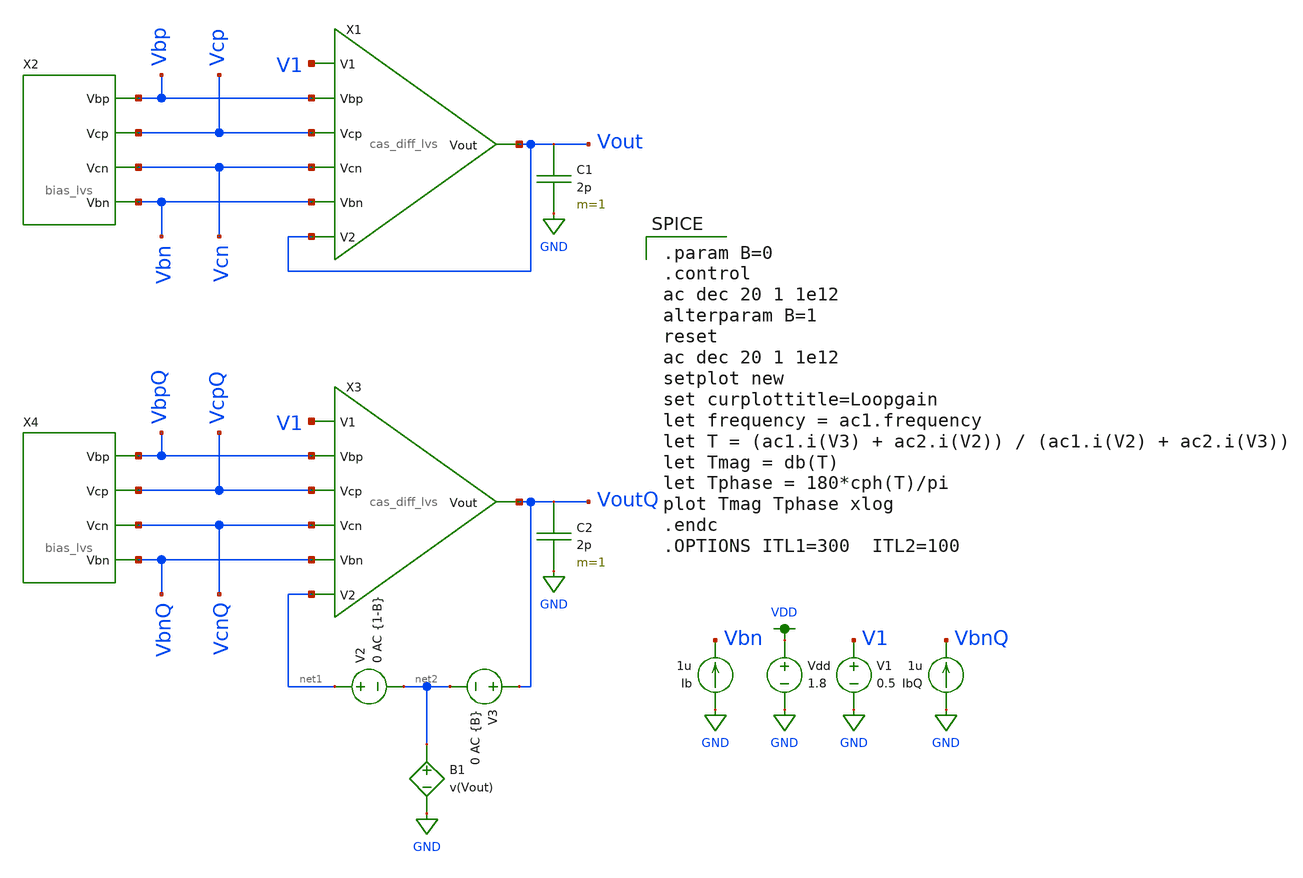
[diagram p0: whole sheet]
** sch_path: mini3/schem/loopgain_noninv.sch
**.subckt loopgain_noninv
X1 V1 Vout Vout Vbp Vcp Vcn Vbn cas_diff_lvs
Vdd VDD GND 1.8
V1 V1 GND 0.5
Ib GND Vbn 1u
C1 Vout GND 2p m=1
X2 Vbp Vcp Vcn Vbn bias_lvs
X3 V1 net1 VoutQ VbpQ VcpQ VcnQ VbnQ cas_diff_lvs
C2 VoutQ GND 2p m=1
X4 VbpQ VcpQ VcnQ VbnQ bias_lvs
IbQ GND VbnQ 1u
V2 net1 net2 0 AC {1-B}
V3 VoutQ net2 0 AC {B}
B1 net2 GND V=v(Vout)
**** begin user architecture code

.option wnflag=1
.lib ~/skywater/skywater-pdk/libraries/sky130_fd_pr_ngspice/latest/models/sky130.lib.spice tt


.param B=0
.control
ac dec 20 1 1e12
alterparam B=1
reset
ac dec 20 1 1e12
setplot new
set curplottitle=Loopgain
let frequency = ac1.frequency
let T = (ac1.i(V3) + ac2.i(V2)) / (ac1.i(V2) + ac2.i(V3))
let Tmag = db(T)
let Tphase = 180*cph(T)/pi
plot Tmag Tphase xlog
.endc
.OPTIONS ITL1=300  ITL2=100

**** end user architecture code
**.ends

* expanding   symbol:  /home/madvlsi/MADVLSI/mini3/schem/cas_diff_lvs.sym # of pins=7
** sym_path: mini3/schem/cas_diff_lvs.sym
** sch_path: mini3/schem/cas_diff_lvs.sch
.subckt cas_diff_lvs V1 V2 Vout Vbp Vcp Vcn Vbn
*.ipin Vbp
*.ipin Vbn
*.ipin Vcn
*.ipin Vcp
*.opin Vout
*.ipin V1
*.ipin V2
XM6a net1 Vcn Vout GND sky130_fd_pr__nfet_01v8 L=0.5 W=6 nf=1 ad='int((nf+1)/2) * W/nf * 0.29' as='int((nf+2)/2) * W/nf * 0.29'
+ pd='2*int((nf+1)/2) * (W/nf + 0.29)' ps='2*int((nf+2)/2) * (W/nf + 0.29)' nrd='0.29 / W' nrs='0.29 / W'
+ sa=0 sb=0 sd=0 mult=1 m=1
XM4a GND Vbn net1 GND sky130_fd_pr__nfet_01v8 L=0.5 W=6 nf=1 ad='int((nf+1)/2) * W/nf * 0.29' as='int((nf+2)/2) * W/nf * 0.29'
+ pd='2*int((nf+1)/2) * (W/nf + 0.29)' ps='2*int((nf+2)/2) * (W/nf + 0.29)' nrd='0.29 / W' nrs='0.29 / W'
+ sa=0 sb=0 sd=0 mult=1 m=1
XM3a net12 Vbn GND GND sky130_fd_pr__nfet_01v8 L=0.5 W=6 nf=1 ad='int((nf+1)/2) * W/nf * 0.29' as='int((nf+2)/2) * W/nf * 0.29'
+ pd='2*int((nf+1)/2) * (W/nf + 0.29)' ps='2*int((nf+2)/2) * (W/nf + 0.29)' nrd='0.29 / W' nrs='0.29 / W'
+ sa=0 sb=0 sd=0 mult=1 m=1
XM5a net2 Vcn net12 GND sky130_fd_pr__nfet_01v8 L=0.5 W=6 nf=1 ad='int((nf+1)/2) * W/nf * 0.29' as='int((nf+2)/2) * W/nf * 0.29'
+ pd='2*int((nf+1)/2) * (W/nf + 0.29)' ps='2*int((nf+2)/2) * (W/nf + 0.29)' nrd='0.29 / W' nrs='0.29 / W'
+ sa=0 sb=0 sd=0 mult=1 m=1
XM5b net12 Vcn net2 GND sky130_fd_pr__nfet_01v8 L=0.5 W=6 nf=1 ad='int((nf+1)/2) * W/nf * 0.29' as='int((nf+2)/2) * W/nf * 0.29'
+ pd='2*int((nf+1)/2) * (W/nf + 0.29)' ps='2*int((nf+2)/2) * (W/nf + 0.29)' nrd='0.29 / W' nrs='0.29 / W'
+ sa=0 sb=0 sd=0 mult=1 m=1
XM3b GND Vbn net12 GND sky130_fd_pr__nfet_01v8 L=0.5 W=6 nf=1 ad='int((nf+1)/2) * W/nf * 0.29' as='int((nf+2)/2) * W/nf * 0.29'
+ pd='2*int((nf+1)/2) * (W/nf + 0.29)' ps='2*int((nf+2)/2) * (W/nf + 0.29)' nrd='0.29 / W' nrs='0.29 / W'
+ sa=0 sb=0 sd=0 mult=1 m=1
XM4b net1 Vbn GND GND sky130_fd_pr__nfet_01v8 L=0.5 W=6 nf=1 ad='int((nf+1)/2) * W/nf * 0.29' as='int((nf+2)/2) * W/nf * 0.29'
+ pd='2*int((nf+1)/2) * (W/nf + 0.29)' ps='2*int((nf+2)/2) * (W/nf + 0.29)' nrd='0.29 / W' nrs='0.29 / W'
+ sa=0 sb=0 sd=0 mult=1 m=1
XM6b Vout Vcn net1 GND sky130_fd_pr__nfet_01v8 L=0.5 W=6 nf=1 ad='int((nf+1)/2) * W/nf * 0.29' as='int((nf+2)/2) * W/nf * 0.29'
+ pd='2*int((nf+1)/2) * (W/nf + 0.29)' ps='2*int((nf+2)/2) * (W/nf + 0.29)' nrd='0.29 / W' nrs='0.29 / W'
+ sa=0 sb=0 sd=0 mult=1 m=1
XM10a Vout Vcp net3 VDD sky130_fd_pr__pfet_01v8 L=0.5 W=6 nf=1 ad='int((nf+1)/2) * W/nf * 0.29' as='int((nf+2)/2) * W/nf * 0.29'
+ pd='2*int((nf+1)/2) * (W/nf + 0.29)' ps='2*int((nf+2)/2) * (W/nf + 0.29)' nrd='0.29 / W' nrs='0.29 / W'
+ sa=0 sb=0 sd=0 mult=1 m=1
XM8a net3 net2 VDD VDD sky130_fd_pr__pfet_01v8 L=0.5 W=6 nf=1 ad='int((nf+1)/2) * W/nf * 0.29' as='int((nf+2)/2) * W/nf * 0.29'
+ pd='2*int((nf+1)/2) * (W/nf + 0.29)' ps='2*int((nf+2)/2) * (W/nf + 0.29)' nrd='0.29 / W' nrs='0.29 / W'
+ sa=0 sb=0 sd=0 mult=1 m=1
XM7a VDD net2 net4 VDD sky130_fd_pr__pfet_01v8 L=0.5 W=6 nf=1 ad='int((nf+1)/2) * W/nf * 0.29' as='int((nf+2)/2) * W/nf * 0.29'
+ pd='2*int((nf+1)/2) * (W/nf + 0.29)' ps='2*int((nf+2)/2) * (W/nf + 0.29)' nrd='0.29 / W' nrs='0.29 / W'
+ sa=0 sb=0 sd=0 mult=1 m=1
XM9a net4 Vcp net2 VDD sky130_fd_pr__pfet_01v8 L=0.5 W=6 nf=1 ad='int((nf+1)/2) * W/nf * 0.29' as='int((nf+2)/2) * W/nf * 0.29'
+ pd='2*int((nf+1)/2) * (W/nf + 0.29)' ps='2*int((nf+2)/2) * (W/nf + 0.29)' nrd='0.29 / W' nrs='0.29 / W'
+ sa=0 sb=0 sd=0 mult=1 m=1
XM9b net2 Vcp net5 VDD sky130_fd_pr__pfet_01v8 L=0.5 W=6 nf=1 ad='int((nf+1)/2) * W/nf * 0.29' as='int((nf+2)/2) * W/nf * 0.29'
+ pd='2*int((nf+1)/2) * (W/nf + 0.29)' ps='2*int((nf+2)/2) * (W/nf + 0.29)' nrd='0.29 / W' nrs='0.29 / W'
+ sa=0 sb=0 sd=0 mult=1 m=1
XM7b net5 net2 VDD VDD sky130_fd_pr__pfet_01v8 L=0.5 W=6 nf=1 ad='int((nf+1)/2) * W/nf * 0.29' as='int((nf+2)/2) * W/nf * 0.29'
+ pd='2*int((nf+1)/2) * (W/nf + 0.29)' ps='2*int((nf+2)/2) * (W/nf + 0.29)' nrd='0.29 / W' nrs='0.29 / W'
+ sa=0 sb=0 sd=0 mult=1 m=1
XM8b VDD net2 net6 VDD sky130_fd_pr__pfet_01v8 L=0.5 W=6 nf=1 ad='int((nf+1)/2) * W/nf * 0.29' as='int((nf+2)/2) * W/nf * 0.29'
+ pd='2*int((nf+1)/2) * (W/nf + 0.29)' ps='2*int((nf+2)/2) * (W/nf + 0.29)' nrd='0.29 / W' nrs='0.29 / W'
+ sa=0 sb=0 sd=0 mult=1 m=1
XM10b net6 Vcp Vout VDD sky130_fd_pr__pfet_01v8 L=0.5 W=6 nf=1 ad='int((nf+1)/2) * W/nf * 0.29' as='int((nf+2)/2) * W/nf * 0.29'
+ pd='2*int((nf+1)/2) * (W/nf + 0.29)' ps='2*int((nf+2)/2) * (W/nf + 0.29)' nrd='0.29 / W' nrs='0.29 / W'
+ sa=0 sb=0 sd=0 mult=1 m=1
XMb1 VDD Vbp net7 VDD sky130_fd_pr__pfet_01v8 L=0.5 W=6 nf=1 ad='int((nf+1)/2) * W/nf * 0.29' as='int((nf+2)/2) * W/nf * 0.29'
+ pd='2*int((nf+1)/2) * (W/nf + 0.29)' ps='2*int((nf+2)/2) * (W/nf + 0.29)' nrd='0.29 / W' nrs='0.29 / W'
+ sa=0 sb=0 sd=0 mult=1 m=1
XMb2 net7 Vbp net8 VDD sky130_fd_pr__pfet_01v8 L=0.5 W=6 nf=1 ad='int((nf+1)/2) * W/nf * 0.29' as='int((nf+2)/2) * W/nf * 0.29'
+ pd='2*int((nf+1)/2) * (W/nf + 0.29)' ps='2*int((nf+2)/2) * (W/nf + 0.29)' nrd='0.29 / W' nrs='0.29 / W'
+ sa=0 sb=0 sd=0 mult=1 m=1
XMb3 net8 Vbp net9 VDD sky130_fd_pr__pfet_01v8 L=0.5 W=6 nf=1 ad='int((nf+1)/2) * W/nf * 0.29' as='int((nf+2)/2) * W/nf * 0.29'
+ pd='2*int((nf+1)/2) * (W/nf + 0.29)' ps='2*int((nf+2)/2) * (W/nf + 0.29)' nrd='0.29 / W' nrs='0.29 / W'
+ sa=0 sb=0 sd=0 mult=1 m=1
XMb4 net9 Vbp VDD VDD sky130_fd_pr__pfet_01v8 L=0.5 W=6 nf=1 ad='int((nf+1)/2) * W/nf * 0.29' as='int((nf+2)/2) * W/nf * 0.29'
+ pd='2*int((nf+1)/2) * (W/nf + 0.29)' ps='2*int((nf+2)/2) * (W/nf + 0.29)' nrd='0.29 / W' nrs='0.29 / W'
+ sa=0 sb=0 sd=0 mult=1 m=1
XMb5 VDD Vbp net10 VDD sky130_fd_pr__pfet_01v8 L=0.5 W=6 nf=1 ad='int((nf+1)/2) * W/nf * 0.29' as='int((nf+2)/2) * W/nf * 0.29'
+ pd='2*int((nf+1)/2) * (W/nf + 0.29)' ps='2*int((nf+2)/2) * (W/nf + 0.29)' nrd='0.29 / W' nrs='0.29 / W'
+ sa=0 sb=0 sd=0 mult=1 m=1
XMb6 net10 Vbp net8 VDD sky130_fd_pr__pfet_01v8 L=0.5 W=6 nf=1 ad='int((nf+1)/2) * W/nf * 0.29' as='int((nf+2)/2) * W/nf * 0.29'
+ pd='2*int((nf+1)/2) * (W/nf + 0.29)' ps='2*int((nf+2)/2) * (W/nf + 0.29)' nrd='0.29 / W' nrs='0.29 / W'
+ sa=0 sb=0 sd=0 mult=1 m=1
XMb7 net8 Vbp net11 VDD sky130_fd_pr__pfet_01v8 L=0.5 W=6 nf=1 ad='int((nf+1)/2) * W/nf * 0.29' as='int((nf+2)/2) * W/nf * 0.29'
+ pd='2*int((nf+1)/2) * (W/nf + 0.29)' ps='2*int((nf+2)/2) * (W/nf + 0.29)' nrd='0.29 / W' nrs='0.29 / W'
+ sa=0 sb=0 sd=0 mult=1 m=1
XMb8 net11 Vbp VDD VDD sky130_fd_pr__pfet_01v8 L=0.5 W=6 nf=1 ad='int((nf+1)/2) * W/nf * 0.29' as='int((nf+2)/2) * W/nf * 0.29'
+ pd='2*int((nf+1)/2) * (W/nf + 0.29)' ps='2*int((nf+2)/2) * (W/nf + 0.29)' nrd='0.29 / W' nrs='0.29 / W'
+ sa=0 sb=0 sd=0 mult=1 m=1
XM1a net13 V1 net8 VDD sky130_fd_pr__pfet_01v8 L=0.5 W=12 nf=1 ad='int((nf+1)/2) * W/nf * 0.29' as='int((nf+2)/2) * W/nf * 0.29'
+ pd='2*int((nf+1)/2) * (W/nf + 0.29)' ps='2*int((nf+2)/2) * (W/nf + 0.29)' nrd='0.29 / W' nrs='0.29 / W'
+ sa=0 sb=0 sd=0 mult=1 m=1
XM1b net12 V1 net13 VDD sky130_fd_pr__pfet_01v8 L=0.5 W=12 nf=1 ad='int((nf+1)/2) * W/nf * 0.29' as='int((nf+2)/2) * W/nf * 0.29'
+ pd='2*int((nf+1)/2) * (W/nf + 0.29)' ps='2*int((nf+2)/2) * (W/nf + 0.29)' nrd='0.29 / W' nrs='0.29 / W'
+ sa=0 sb=0 sd=0 mult=1 m=1
XM2a net1 V2 net15 VDD sky130_fd_pr__pfet_01v8 L=0.5 W=12 nf=1 ad='int((nf+1)/2) * W/nf * 0.29' as='int((nf+2)/2) * W/nf * 0.29'
+ pd='2*int((nf+1)/2) * (W/nf + 0.29)' ps='2*int((nf+2)/2) * (W/nf + 0.29)' nrd='0.29 / W' nrs='0.29 / W'
+ sa=0 sb=0 sd=0 mult=1 m=1
XM2b net15 V2 net8 VDD sky130_fd_pr__pfet_01v8 L=0.5 W=12 nf=1 ad='int((nf+1)/2) * W/nf * 0.29' as='int((nf+2)/2) * W/nf * 0.29'
+ pd='2*int((nf+1)/2) * (W/nf + 0.29)' ps='2*int((nf+2)/2) * (W/nf + 0.29)' nrd='0.29 / W' nrs='0.29 / W'
+ sa=0 sb=0 sd=0 mult=1 m=1
XM2c net8 V2 net16 VDD sky130_fd_pr__pfet_01v8 L=0.5 W=12 nf=1 ad='int((nf+1)/2) * W/nf * 0.29' as='int((nf+2)/2) * W/nf * 0.29'
+ pd='2*int((nf+1)/2) * (W/nf + 0.29)' ps='2*int((nf+2)/2) * (W/nf + 0.29)' nrd='0.29 / W' nrs='0.29 / W'
+ sa=0 sb=0 sd=0 mult=1 m=1
XM2d net16 V2 net1 VDD sky130_fd_pr__pfet_01v8 L=0.5 W=12 nf=1 ad='int((nf+1)/2) * W/nf * 0.29' as='int((nf+2)/2) * W/nf * 0.29'
+ pd='2*int((nf+1)/2) * (W/nf + 0.29)' ps='2*int((nf+2)/2) * (W/nf + 0.29)' nrd='0.29 / W' nrs='0.29 / W'
+ sa=0 sb=0 sd=0 mult=1 m=1
XM1c net14 V1 net12 VDD sky130_fd_pr__pfet_01v8 L=0.5 W=12 nf=1 ad='int((nf+1)/2) * W/nf * 0.29' as='int((nf+2)/2) * W/nf * 0.29'
+ pd='2*int((nf+1)/2) * (W/nf + 0.29)' ps='2*int((nf+2)/2) * (W/nf + 0.29)' nrd='0.29 / W' nrs='0.29 / W'
+ sa=0 sb=0 sd=0 mult=1 m=1
XM1d net8 V1 net14 VDD sky130_fd_pr__pfet_01v8 L=0.5 W=12 nf=1 ad='int((nf+1)/2) * W/nf * 0.29' as='int((nf+2)/2) * W/nf * 0.29'
+ pd='2*int((nf+1)/2) * (W/nf + 0.29)' ps='2*int((nf+2)/2) * (W/nf + 0.29)' nrd='0.29 / W' nrs='0.29 / W'
+ sa=0 sb=0 sd=0 mult=1 m=1
XMdmb3 VDD VDD Vout VDD sky130_fd_pr__pfet_01v8 L=0.5 W=6 nf=1 ad='int((nf+1)/2) * W/nf * 0.29' as='int((nf+2)/2) * W/nf * 0.29'
+ pd='2*int((nf+1)/2) * (W/nf + 0.29)' ps='2*int((nf+2)/2) * (W/nf + 0.29)' nrd='0.29 / W' nrs='0.29 / W'
+ sa=0 sb=0 sd=0 mult=1 m=1
XMdmb2 VDD VDD net1 VDD sky130_fd_pr__pfet_01v8 L=0.5 W=12 nf=1 ad='int((nf+1)/2) * W/nf * 0.29' as='int((nf+2)/2) * W/nf * 0.29'
+ pd='2*int((nf+1)/2) * (W/nf + 0.29)' ps='2*int((nf+2)/2) * (W/nf + 0.29)' nrd='0.29 / W' nrs='0.29 / W'
+ sa=0 sb=0 sd=0 mult=1 m=1
XMdmb1 VDD VDD VDD VDD sky130_fd_pr__pfet_01v8 L=0.5 W=6 nf=1 ad='int((nf+1)/2) * W/nf * 0.29' as='int((nf+2)/2) * W/nf * 0.29'
+ pd='2*int((nf+1)/2) * (W/nf + 0.29)' ps='2*int((nf+2)/2) * (W/nf + 0.29)' nrd='0.29 / W' nrs='0.29 / W'
+ sa=0 sb=0 sd=0 mult=1 m=1
XMdmb7 Vout VDD VDD VDD sky130_fd_pr__pfet_01v8 L=0.5 W=6 nf=1 ad='int((nf+1)/2) * W/nf * 0.29' as='int((nf+2)/2) * W/nf * 0.29'
+ pd='2*int((nf+1)/2) * (W/nf + 0.29)' ps='2*int((nf+2)/2) * (W/nf + 0.29)' nrd='0.29 / W' nrs='0.29 / W'
+ sa=0 sb=0 sd=0 mult=1 m=1
XMdmb6 net1 VDD VDD VDD sky130_fd_pr__pfet_01v8 L=0.5 W=12 nf=1 ad='int((nf+1)/2) * W/nf * 0.29' as='int((nf+2)/2) * W/nf * 0.29'
+ pd='2*int((nf+1)/2) * (W/nf + 0.29)' ps='2*int((nf+2)/2) * (W/nf + 0.29)' nrd='0.29 / W' nrs='0.29 / W'
+ sa=0 sb=0 sd=0 mult=1 m=1
XMdmb5 VDD VDD VDD VDD sky130_fd_pr__pfet_01v8 L=0.5 W=6 nf=1 ad='int((nf+1)/2) * W/nf * 0.29' as='int((nf+2)/2) * W/nf * 0.29'
+ pd='2*int((nf+1)/2) * (W/nf + 0.29)' ps='2*int((nf+2)/2) * (W/nf + 0.29)' nrd='0.29 / W' nrs='0.29 / W'
+ sa=0 sb=0 sd=0 mult=1 m=1
XMdmb4 Vout GND GND GND sky130_fd_pr__nfet_01v8 L=0.5 W=6 nf=1 ad='int((nf+1)/2) * W/nf * 0.29' as='int((nf+2)/2) * W/nf * 0.29'
+ pd='2*int((nf+1)/2) * (W/nf + 0.29)' ps='2*int((nf+2)/2) * (W/nf + 0.29)' nrd='0.29 / W' nrs='0.29 / W'
+ sa=0 sb=0 sd=0 mult=1 m=1
XMdmb8 GND GND Vout GND sky130_fd_pr__nfet_01v8 L=0.5 W=6 nf=1 ad='int((nf+1)/2) * W/nf * 0.29' as='int((nf+2)/2) * W/nf * 0.29'
+ pd='2*int((nf+1)/2) * (W/nf + 0.29)' ps='2*int((nf+2)/2) * (W/nf + 0.29)' nrd='0.29 / W' nrs='0.29 / W'
+ sa=0 sb=0 sd=0 mult=1 m=1
.ends


* expanding   symbol:  /home/madvlsi/MADVLSI/mini3/schem/bias_lvs.sym # of pins=4
** sym_path: mini3/schem/bias_lvs.sym
** sch_path: mini3/schem/bias_lvs.sch
.subckt bias_lvs Vbp Vcp Vcn Vbn
*.opin Vcn
*.opin Vcp
*.opin Vbp
*.iopin Vbn
XM4a net15 Vbn net1 GND sky130_fd_pr__nfet_01v8 L=0.5 W=6 nf=1 ad='int((nf+1)/2) * W/nf * 0.29' as='int((nf+2)/2) * W/nf * 0.29'
+ pd='2*int((nf+1)/2) * (W/nf + 0.29)' ps='2*int((nf+2)/2) * (W/nf + 0.29)' nrd='0.29 / W' nrs='0.29 / W'
+ sa=0 sb=0 sd=0 mult=1 m=1
XM4b net1 Vbn net2 GND sky130_fd_pr__nfet_01v8 L=0.5 W=6 nf=1 ad='int((nf+1)/2) * W/nf * 0.29' as='int((nf+2)/2) * W/nf * 0.29'
+ pd='2*int((nf+1)/2) * (W/nf + 0.29)' ps='2*int((nf+2)/2) * (W/nf + 0.29)' nrd='0.29 / W' nrs='0.29 / W'
+ sa=0 sb=0 sd=0 mult=1 m=1
XM4c net2 Vbn GND GND sky130_fd_pr__nfet_01v8 L=0.5 W=6 nf=1 ad='int((nf+1)/2) * W/nf * 0.29' as='int((nf+2)/2) * W/nf * 0.29'
+ pd='2*int((nf+1)/2) * (W/nf + 0.29)' ps='2*int((nf+2)/2) * (W/nf + 0.29)' nrd='0.29 / W' nrs='0.29 / W'
+ sa=0 sb=0 sd=0 mult=1 m=1
XM5a GND Vbn Vcp GND sky130_fd_pr__nfet_01v8 L=0.5 W=6 nf=1 ad='int((nf+1)/2) * W/nf * 0.29' as='int((nf+2)/2) * W/nf * 0.29'
+ pd='2*int((nf+1)/2) * (W/nf + 0.29)' ps='2*int((nf+2)/2) * (W/nf + 0.29)' nrd='0.29 / W' nrs='0.29 / W'
+ sa=0 sb=0 sd=0 mult=1 m=1
XM5b Vcp Vbn GND GND sky130_fd_pr__nfet_01v8 L=0.5 W=6 nf=1 ad='int((nf+1)/2) * W/nf * 0.29' as='int((nf+2)/2) * W/nf * 0.29'
+ pd='2*int((nf+1)/2) * (W/nf + 0.29)' ps='2*int((nf+2)/2) * (W/nf + 0.29)' nrd='0.29 / W' nrs='0.29 / W'
+ sa=0 sb=0 sd=0 mult=1 m=1
XM4d GND Vbn net3 GND sky130_fd_pr__nfet_01v8 L=0.5 W=6 nf=1 ad='int((nf+1)/2) * W/nf * 0.29' as='int((nf+2)/2) * W/nf * 0.29'
+ pd='2*int((nf+1)/2) * (W/nf + 0.29)' ps='2*int((nf+2)/2) * (W/nf + 0.29)' nrd='0.29 / W' nrs='0.29 / W'
+ sa=0 sb=0 sd=0 mult=1 m=1
XM4e net3 Vbn net7 GND sky130_fd_pr__nfet_01v8 L=0.5 W=6 nf=1 ad='int((nf+1)/2) * W/nf * 0.29' as='int((nf+2)/2) * W/nf * 0.29'
+ pd='2*int((nf+1)/2) * (W/nf + 0.29)' ps='2*int((nf+2)/2) * (W/nf + 0.29)' nrd='0.29 / W' nrs='0.29 / W'
+ sa=0 sb=0 sd=0 mult=1 m=1
XM4f net7 Vbn net15 GND sky130_fd_pr__nfet_01v8 L=0.5 W=6 nf=1 ad='int((nf+1)/2) * W/nf * 0.29' as='int((nf+2)/2) * W/nf * 0.29'
+ pd='2*int((nf+1)/2) * (W/nf + 0.29)' ps='2*int((nf+2)/2) * (W/nf + 0.29)' nrd='0.29 / W' nrs='0.29 / W'
+ sa=0 sb=0 sd=0 mult=1 m=1
XM1a VDD net15 net4 VDD sky130_fd_pr__pfet_01v8 L=0.5 W=6 nf=1 ad='int((nf+1)/2) * W/nf * 0.29' as='int((nf+2)/2) * W/nf * 0.29'
+ pd='2*int((nf+1)/2) * (W/nf + 0.29)' ps='2*int((nf+2)/2) * (W/nf + 0.29)' nrd='0.29 / W' nrs='0.29 / W'
+ sa=0 sb=0 sd=0 mult=1 m=1
XM2a net4 net15 net5 VDD sky130_fd_pr__pfet_01v8 L=0.5 W=6 nf=1 ad='int((nf+1)/2) * W/nf * 0.29' as='int((nf+2)/2) * W/nf * 0.29'
+ pd='2*int((nf+1)/2) * (W/nf + 0.29)' ps='2*int((nf+2)/2) * (W/nf + 0.29)' nrd='0.29 / W' nrs='0.29 / W'
+ sa=0 sb=0 sd=0 mult=1 m=1
XM2b net5 net15 net4 VDD sky130_fd_pr__pfet_01v8 L=0.5 W=6 nf=1 ad='int((nf+1)/2) * W/nf * 0.29' as='int((nf+2)/2) * W/nf * 0.29'
+ pd='2*int((nf+1)/2) * (W/nf + 0.29)' ps='2*int((nf+2)/2) * (W/nf + 0.29)' nrd='0.29 / W' nrs='0.29 / W'
+ sa=0 sb=0 sd=0 mult=1 m=1
XM3a net4 Vcp Vcp VDD sky130_fd_pr__pfet_01v8 L=0.5 W=6 nf=1 ad='int((nf+1)/2) * W/nf * 0.29' as='int((nf+2)/2) * W/nf * 0.29'
+ pd='2*int((nf+1)/2) * (W/nf + 0.29)' ps='2*int((nf+2)/2) * (W/nf + 0.29)' nrd='0.29 / W' nrs='0.29 / W'
+ sa=0 sb=0 sd=0 mult=1 m=1
XM3b Vcp Vcp net4 VDD sky130_fd_pr__pfet_01v8 L=0.5 W=6 nf=1 ad='int((nf+1)/2) * W/nf * 0.29' as='int((nf+2)/2) * W/nf * 0.29'
+ pd='2*int((nf+1)/2) * (W/nf + 0.29)' ps='2*int((nf+2)/2) * (W/nf + 0.29)' nrd='0.29 / W' nrs='0.29 / W'
+ sa=0 sb=0 sd=0 mult=1 m=1
XM2c net4 net15 net6 VDD sky130_fd_pr__pfet_01v8 L=0.5 W=6 nf=1 ad='int((nf+1)/2) * W/nf * 0.29' as='int((nf+2)/2) * W/nf * 0.29'
+ pd='2*int((nf+1)/2) * (W/nf + 0.29)' ps='2*int((nf+2)/2) * (W/nf + 0.29)' nrd='0.29 / W' nrs='0.29 / W'
+ sa=0 sb=0 sd=0 mult=1 m=1
XM2d net6 net15 net4 VDD sky130_fd_pr__pfet_01v8 L=0.5 W=6 nf=1 ad='int((nf+1)/2) * W/nf * 0.29' as='int((nf+2)/2) * W/nf * 0.29'
+ pd='2*int((nf+1)/2) * (W/nf + 0.29)' ps='2*int((nf+2)/2) * (W/nf + 0.29)' nrd='0.29 / W' nrs='0.29 / W'
+ sa=0 sb=0 sd=0 mult=1 m=1
XM1b net4 net15 VDD VDD sky130_fd_pr__pfet_01v8 L=0.5 W=6 nf=1 ad='int((nf+1)/2) * W/nf * 0.29' as='int((nf+2)/2) * W/nf * 0.29'
+ pd='2*int((nf+1)/2) * (W/nf + 0.29)' ps='2*int((nf+2)/2) * (W/nf + 0.29)' nrd='0.29 / W' nrs='0.29 / W'
+ sa=0 sb=0 sd=0 mult=1 m=1
XM6a net16 Vbp net8 VDD sky130_fd_pr__pfet_01v8 L=0.5 W=6 nf=1 ad='int((nf+1)/2) * W/nf * 0.29' as='int((nf+2)/2) * W/nf * 0.29'
+ pd='2*int((nf+1)/2) * (W/nf + 0.29)' ps='2*int((nf+2)/2) * (W/nf + 0.29)' nrd='0.29 / W' nrs='0.29 / W'
+ sa=0 sb=0 sd=0 mult=1 m=1
XM6b net8 Vbp net9 VDD sky130_fd_pr__pfet_01v8 L=0.5 W=6 nf=1 ad='int((nf+1)/2) * W/nf * 0.29' as='int((nf+2)/2) * W/nf * 0.29'
+ pd='2*int((nf+1)/2) * (W/nf + 0.29)' ps='2*int((nf+2)/2) * (W/nf + 0.29)' nrd='0.29 / W' nrs='0.29 / W'
+ sa=0 sb=0 sd=0 mult=1 m=1
XM6c net9 Vbp VDD VDD sky130_fd_pr__pfet_01v8 L=0.5 W=6 nf=1 ad='int((nf+1)/2) * W/nf * 0.29' as='int((nf+2)/2) * W/nf * 0.29'
+ pd='2*int((nf+1)/2) * (W/nf + 0.29)' ps='2*int((nf+2)/2) * (W/nf + 0.29)' nrd='0.29 / W' nrs='0.29 / W'
+ sa=0 sb=0 sd=0 mult=1 m=1
XM7a VDD Vbp Vcn VDD sky130_fd_pr__pfet_01v8 L=0.5 W=6 nf=1 ad='int((nf+1)/2) * W/nf * 0.29' as='int((nf+2)/2) * W/nf * 0.29'
+ pd='2*int((nf+1)/2) * (W/nf + 0.29)' ps='2*int((nf+2)/2) * (W/nf + 0.29)' nrd='0.29 / W' nrs='0.29 / W'
+ sa=0 sb=0 sd=0 mult=1 m=1
XM7b Vcn Vbp VDD VDD sky130_fd_pr__pfet_01v8 L=0.5 W=6 nf=1 ad='int((nf+1)/2) * W/nf * 0.29' as='int((nf+2)/2) * W/nf * 0.29'
+ pd='2*int((nf+1)/2) * (W/nf + 0.29)' ps='2*int((nf+2)/2) * (W/nf + 0.29)' nrd='0.29 / W' nrs='0.29 / W'
+ sa=0 sb=0 sd=0 mult=1 m=1
XM6d VDD Vbp net10 VDD sky130_fd_pr__pfet_01v8 L=0.5 W=6 nf=1 ad='int((nf+1)/2) * W/nf * 0.29' as='int((nf+2)/2) * W/nf * 0.29'
+ pd='2*int((nf+1)/2) * (W/nf + 0.29)' ps='2*int((nf+2)/2) * (W/nf + 0.29)' nrd='0.29 / W' nrs='0.29 / W'
+ sa=0 sb=0 sd=0 mult=1 m=1
XM6e net10 Vbp net11 VDD sky130_fd_pr__pfet_01v8 L=0.5 W=6 nf=1 ad='int((nf+1)/2) * W/nf * 0.29' as='int((nf+2)/2) * W/nf * 0.29'
+ pd='2*int((nf+1)/2) * (W/nf + 0.29)' ps='2*int((nf+2)/2) * (W/nf + 0.29)' nrd='0.29 / W' nrs='0.29 / W'
+ sa=0 sb=0 sd=0 mult=1 m=1
XM6f net11 Vbp net16 VDD sky130_fd_pr__pfet_01v8 L=0.5 W=6 nf=1 ad='int((nf+1)/2) * W/nf * 0.29' as='int((nf+2)/2) * W/nf * 0.29'
+ pd='2*int((nf+1)/2) * (W/nf + 0.29)' ps='2*int((nf+2)/2) * (W/nf + 0.29)' nrd='0.29 / W' nrs='0.29 / W'
+ sa=0 sb=0 sd=0 mult=1 m=1
XM10a net12 net16 GND GND sky130_fd_pr__nfet_01v8 L=0.5 W=6 nf=1 ad='int((nf+1)/2) * W/nf * 0.29' as='int((nf+2)/2) * W/nf * 0.29'
+ pd='2*int((nf+1)/2) * (W/nf + 0.29)' ps='2*int((nf+2)/2) * (W/nf + 0.29)' nrd='0.29 / W' nrs='0.29 / W'
+ sa=0 sb=0 sd=0 mult=1 m=1
XM8a net13 net16 net12 GND sky130_fd_pr__nfet_01v8 L=0.5 W=6 nf=1 ad='int((nf+1)/2) * W/nf * 0.29' as='int((nf+2)/2) * W/nf * 0.29'
+ pd='2*int((nf+1)/2) * (W/nf + 0.29)' ps='2*int((nf+2)/2) * (W/nf + 0.29)' nrd='0.29 / W' nrs='0.29 / W'
+ sa=0 sb=0 sd=0 mult=1 m=1
XM8b net12 net16 net13 GND sky130_fd_pr__nfet_01v8 L=0.5 W=6 nf=1 ad='int((nf+1)/2) * W/nf * 0.29' as='int((nf+2)/2) * W/nf * 0.29'
+ pd='2*int((nf+1)/2) * (W/nf + 0.29)' ps='2*int((nf+2)/2) * (W/nf + 0.29)' nrd='0.29 / W' nrs='0.29 / W'
+ sa=0 sb=0 sd=0 mult=1 m=1
XM9a Vcn Vcn net12 GND sky130_fd_pr__nfet_01v8 L=0.5 W=6 nf=1 ad='int((nf+1)/2) * W/nf * 0.29' as='int((nf+2)/2) * W/nf * 0.29'
+ pd='2*int((nf+1)/2) * (W/nf + 0.29)' ps='2*int((nf+2)/2) * (W/nf + 0.29)' nrd='0.29 / W' nrs='0.29 / W'
+ sa=0 sb=0 sd=0 mult=1 m=1
XM9b net12 Vcn Vcn GND sky130_fd_pr__nfet_01v8 L=0.5 W=6 nf=1 ad='int((nf+1)/2) * W/nf * 0.29' as='int((nf+2)/2) * W/nf * 0.29'
+ pd='2*int((nf+1)/2) * (W/nf + 0.29)' ps='2*int((nf+2)/2) * (W/nf + 0.29)' nrd='0.29 / W' nrs='0.29 / W'
+ sa=0 sb=0 sd=0 mult=1 m=1
XM8c net14 net16 net12 GND sky130_fd_pr__nfet_01v8 L=0.5 W=6 nf=1 ad='int((nf+1)/2) * W/nf * 0.29' as='int((nf+2)/2) * W/nf * 0.29'
+ pd='2*int((nf+1)/2) * (W/nf + 0.29)' ps='2*int((nf+2)/2) * (W/nf + 0.29)' nrd='0.29 / W' nrs='0.29 / W'
+ sa=0 sb=0 sd=0 mult=1 m=1
XM8d net12 net16 net14 GND sky130_fd_pr__nfet_01v8 L=0.5 W=6 nf=1 ad='int((nf+1)/2) * W/nf * 0.29' as='int((nf+2)/2) * W/nf * 0.29'
+ pd='2*int((nf+1)/2) * (W/nf + 0.29)' ps='2*int((nf+2)/2) * (W/nf + 0.29)' nrd='0.29 / W' nrs='0.29 / W'
+ sa=0 sb=0 sd=0 mult=1 m=1
XM10b GND net16 net12 GND sky130_fd_pr__nfet_01v8 L=0.5 W=6 nf=1 ad='int((nf+1)/2) * W/nf * 0.29' as='int((nf+2)/2) * W/nf * 0.29'
+ pd='2*int((nf+1)/2) * (W/nf + 0.29)' ps='2*int((nf+2)/2) * (W/nf + 0.29)' nrd='0.29 / W' nrs='0.29 / W'
+ sa=0 sb=0 sd=0 mult=1 m=1
XM23 VDD VDD VDD VDD sky130_fd_pr__pfet_01v8 L=0.5 W=6 nf=1 ad='int((nf+1)/2) * W/nf * 0.29' as='int((nf+2)/2) * W/nf * 0.29'
+ pd='2*int((nf+1)/2) * (W/nf + 0.29)' ps='2*int((nf+2)/2) * (W/nf + 0.29)' nrd='0.29 / W' nrs='0.29 / W'
+ sa=0 sb=0 sd=0 mult=1 m=1
XM32 net15 GND GND GND sky130_fd_pr__nfet_01v8 L=0.5 W=6 nf=1 ad='int((nf+1)/2) * W/nf * 0.29' as='int((nf+2)/2) * W/nf * 0.29'
+ pd='2*int((nf+1)/2) * (W/nf + 0.29)' ps='2*int((nf+2)/2) * (W/nf + 0.29)' nrd='0.29 / W' nrs='0.29 / W'
+ sa=0 sb=0 sd=0 mult=1 m=1
XM33 GND GND net15 GND sky130_fd_pr__nfet_01v8 L=0.5 W=6 nf=1 ad='int((nf+1)/2) * W/nf * 0.29' as='int((nf+2)/2) * W/nf * 0.29'
+ pd='2*int((nf+1)/2) * (W/nf + 0.29)' ps='2*int((nf+2)/2) * (W/nf + 0.29)' nrd='0.29 / W' nrs='0.29 / W'
+ sa=0 sb=0 sd=0 mult=1 m=1
XM42 VDD VDD net16 VDD sky130_fd_pr__pfet_01v8 L=0.5 W=6 nf=1 ad='int((nf+1)/2) * W/nf * 0.29' as='int((nf+2)/2) * W/nf * 0.29'
+ pd='2*int((nf+1)/2) * (W/nf + 0.29)' ps='2*int((nf+2)/2) * (W/nf + 0.29)' nrd='0.29 / W' nrs='0.29 / W'
+ sa=0 sb=0 sd=0 mult=1 m=1
XM43 net16 VDD VDD VDD sky130_fd_pr__pfet_01v8 L=0.5 W=6 nf=1 ad='int((nf+1)/2) * W/nf * 0.29' as='int((nf+2)/2) * W/nf * 0.29'
+ pd='2*int((nf+1)/2) * (W/nf + 0.29)' ps='2*int((nf+2)/2) * (W/nf + 0.29)' nrd='0.29 / W' nrs='0.29 / W'
+ sa=0 sb=0 sd=0 mult=1 m=1
XM52 GND GND GND GND sky130_fd_pr__nfet_01v8 L=0.5 W=6 nf=1 ad='int((nf+1)/2) * W/nf * 0.29' as='int((nf+2)/2) * W/nf * 0.29'
+ pd='2*int((nf+1)/2) * (W/nf + 0.29)' ps='2*int((nf+2)/2) * (W/nf + 0.29)' nrd='0.29 / W' nrs='0.29 / W'
+ sa=0 sb=0 sd=0 mult=1 m=1
XM53 GND GND GND GND sky130_fd_pr__nfet_01v8 L=0.5 W=6 nf=1 ad='int((nf+1)/2) * W/nf * 0.29' as='int((nf+2)/2) * W/nf * 0.29'
+ pd='2*int((nf+1)/2) * (W/nf + 0.29)' ps='2*int((nf+2)/2) * (W/nf + 0.29)' nrd='0.29 / W' nrs='0.29 / W'
+ sa=0 sb=0 sd=0 mult=1 m=1
XM21 VDD VDD VDD VDD sky130_fd_pr__pfet_01v8 L=0.5 W=6 nf=1 ad='int((nf+1)/2) * W/nf * 0.29' as='int((nf+2)/2) * W/nf * 0.29'
+ pd='2*int((nf+1)/2) * (W/nf + 0.29)' ps='2*int((nf+2)/2) * (W/nf + 0.29)' nrd='0.29 / W' nrs='0.29 / W'
+ sa=0 sb=0 sd=0 mult=1 m=1
XM1 Vbn Vbn GND GND sky130_fd_pr__nfet_01v8 L=0.5 W=6 nf=1 ad='int((nf+1)/2) * W/nf * 0.29' as='int((nf+2)/2) * W/nf * 0.29'
+ pd='2*int((nf+1)/2) * (W/nf + 0.29)' ps='2*int((nf+2)/2) * (W/nf + 0.29)' nrd='0.29 / W' nrs='0.29 / W'
+ sa=0 sb=0 sd=0 mult=1 m=1
XM2 GND Vbn Vbp GND sky130_fd_pr__nfet_01v8 L=0.5 W=6 nf=1 ad='int((nf+1)/2) * W/nf * 0.29' as='int((nf+2)/2) * W/nf * 0.29'
+ pd='2*int((nf+1)/2) * (W/nf + 0.29)' ps='2*int((nf+2)/2) * (W/nf + 0.29)' nrd='0.29 / W' nrs='0.29 / W'
+ sa=0 sb=0 sd=0 mult=1 m=1
XM3 VDD Vbp Vbp VDD sky130_fd_pr__pfet_01v8 L=0.5 W=6 nf=1 ad='int((nf+1)/2) * W/nf * 0.29' as='int((nf+2)/2) * W/nf * 0.29'
+ pd='2*int((nf+1)/2) * (W/nf + 0.29)' ps='2*int((nf+2)/2) * (W/nf + 0.29)' nrd='0.29 / W' nrs='0.29 / W'
+ sa=0 sb=0 sd=0 mult=1 m=1
XM4 Vbp Vbn GND GND sky130_fd_pr__nfet_01v8 L=0.5 W=6 nf=1 ad='int((nf+1)/2) * W/nf * 0.29' as='int((nf+2)/2) * W/nf * 0.29'
+ pd='2*int((nf+1)/2) * (W/nf + 0.29)' ps='2*int((nf+2)/2) * (W/nf + 0.29)' nrd='0.29 / W' nrs='0.29 / W'
+ sa=0 sb=0 sd=0 mult=1 m=1
XM5 GND Vbn Vbn GND sky130_fd_pr__nfet_01v8 L=0.5 W=6 nf=1 ad='int((nf+1)/2) * W/nf * 0.29' as='int((nf+2)/2) * W/nf * 0.29'
+ pd='2*int((nf+1)/2) * (W/nf + 0.29)' ps='2*int((nf+2)/2) * (W/nf + 0.29)' nrd='0.29 / W' nrs='0.29 / W'
+ sa=0 sb=0 sd=0 mult=1 m=1
XM6 VDD VDD VDD VDD sky130_fd_pr__pfet_01v8 L=0.5 W=6 nf=1 ad='int((nf+1)/2) * W/nf * 0.29' as='int((nf+2)/2) * W/nf * 0.29'
+ pd='2*int((nf+1)/2) * (W/nf + 0.29)' ps='2*int((nf+2)/2) * (W/nf + 0.29)' nrd='0.29 / W' nrs='0.29 / W'
+ sa=0 sb=0 sd=0 mult=1 m=1
XM7 VDD VDD VDD VDD sky130_fd_pr__pfet_01v8 L=0.5 W=6 nf=1 ad='int((nf+1)/2) * W/nf * 0.29' as='int((nf+2)/2) * W/nf * 0.29'
+ pd='2*int((nf+1)/2) * (W/nf + 0.29)' ps='2*int((nf+2)/2) * (W/nf + 0.29)' nrd='0.29 / W' nrs='0.29 / W'
+ sa=0 sb=0 sd=0 mult=1 m=1
XM8 Vbp Vbp VDD VDD sky130_fd_pr__pfet_01v8 L=0.5 W=6 nf=1 ad='int((nf+1)/2) * W/nf * 0.29' as='int((nf+2)/2) * W/nf * 0.29'
+ pd='2*int((nf+1)/2) * (W/nf + 0.29)' ps='2*int((nf+2)/2) * (W/nf + 0.29)' nrd='0.29 / W' nrs='0.29 / W'
+ sa=0 sb=0 sd=0 mult=1 m=1
XM9 VDD VDD Vbp VDD sky130_fd_pr__pfet_01v8 L=0.5 W=6 nf=1 ad='int((nf+1)/2) * W/nf * 0.29' as='int((nf+2)/2) * W/nf * 0.29'
+ pd='2*int((nf+1)/2) * (W/nf + 0.29)' ps='2*int((nf+2)/2) * (W/nf + 0.29)' nrd='0.29 / W' nrs='0.29 / W'
+ sa=0 sb=0 sd=0 mult=1 m=1
XM10 Vbp GND GND GND sky130_fd_pr__nfet_01v8 L=0.5 W=6 nf=1 ad='int((nf+1)/2) * W/nf * 0.29' as='int((nf+2)/2) * W/nf * 0.29'
+ pd='2*int((nf+1)/2) * (W/nf + 0.29)' ps='2*int((nf+2)/2) * (W/nf + 0.29)' nrd='0.29 / W' nrs='0.29 / W'
+ sa=0 sb=0 sd=0 mult=1 m=1
XM11 Vbp VDD VDD VDD sky130_fd_pr__pfet_01v8 L=0.5 W=6 nf=1 ad='int((nf+1)/2) * W/nf * 0.29' as='int((nf+2)/2) * W/nf * 0.29'
+ pd='2*int((nf+1)/2) * (W/nf + 0.29)' ps='2*int((nf+2)/2) * (W/nf + 0.29)' nrd='0.29 / W' nrs='0.29 / W'
+ sa=0 sb=0 sd=0 mult=1 m=1
XM12 GND GND Vbp GND sky130_fd_pr__nfet_01v8 L=0.5 W=6 nf=1 ad='int((nf+1)/2) * W/nf * 0.29' as='int((nf+2)/2) * W/nf * 0.29'
+ pd='2*int((nf+1)/2) * (W/nf + 0.29)' ps='2*int((nf+2)/2) * (W/nf + 0.29)' nrd='0.29 / W' nrs='0.29 / W'
+ sa=0 sb=0 sd=0 mult=1 m=1
.ends

.GLOBAL VDD
.GLOBAL GND
.end
